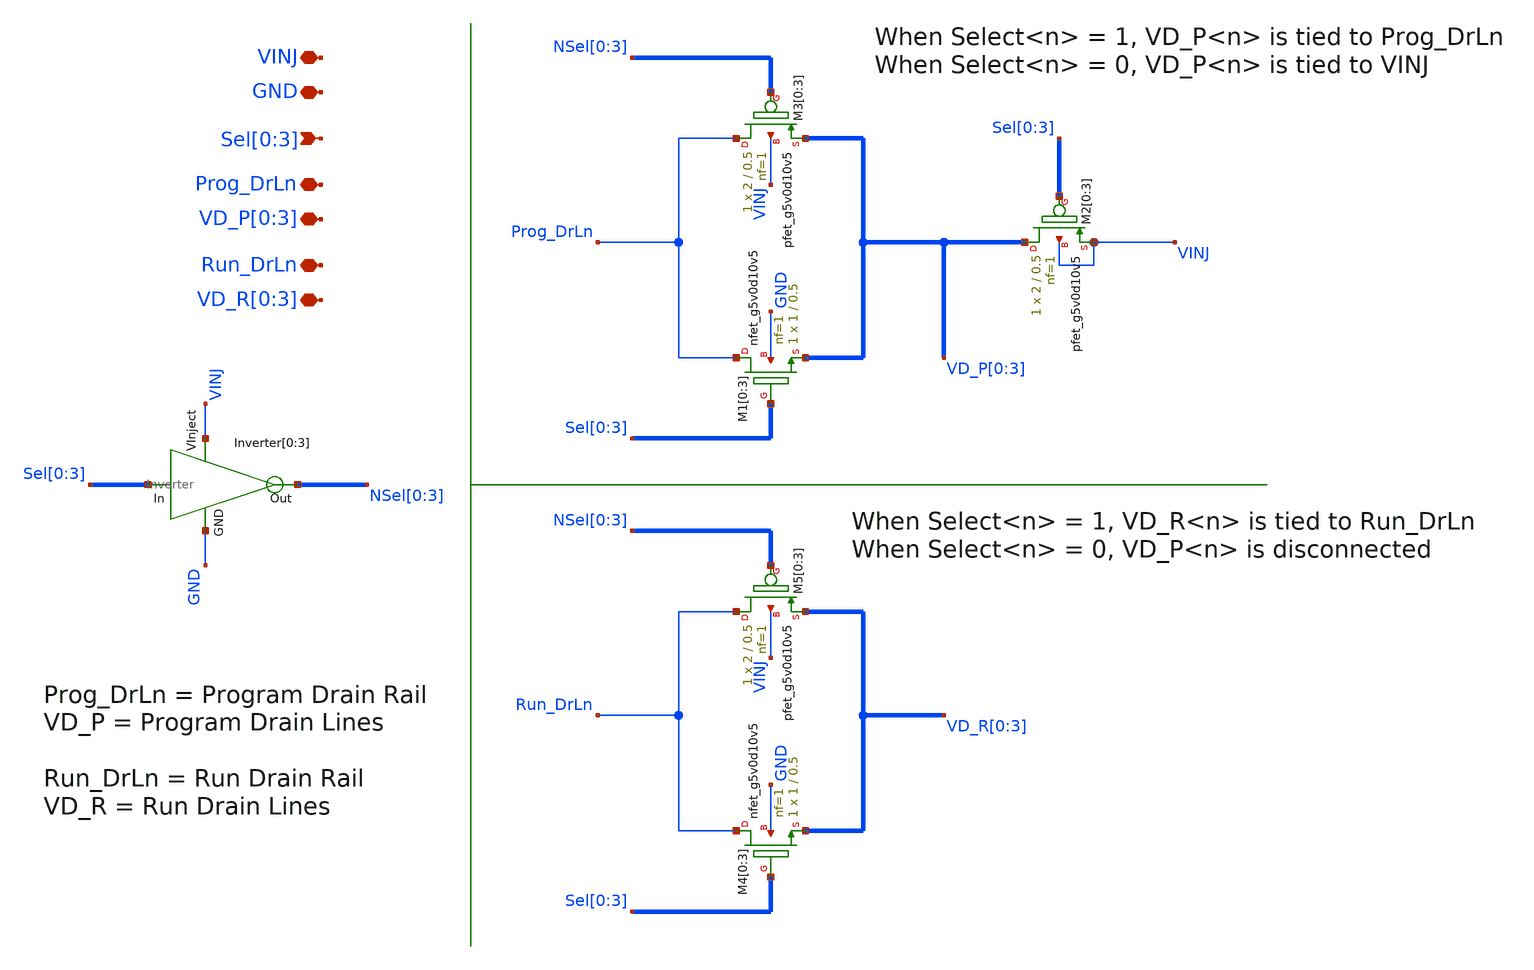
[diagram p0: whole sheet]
** sch_path: sky130_cells/IndirectVMM_DrainSwcs/IndirectVMM_DrainSwcs.sch
**.subckt IndirectVMM_DrainSwcs Sel[0],Sel[1],Sel[2],Sel[3] Prog_DrLn Run_DrLn
*+ VD_P[0],VD_P[1],VD_P[2],VD_P[3] VD_R[0],VD_R[1],VD_R[2],VD_R[3] VINJ GND
*.ipin Sel[0],Sel[1],Sel[2],Sel[3]
*.iopin Prog_DrLn
*.iopin Run_DrLn
*.iopin VD_P[0],VD_P[1],VD_P[2],VD_P[3]
*.iopin VD_R[0],VD_R[1],VD_R[2],VD_R[3]
*.iopin VINJ
*.iopin GND
Inverter[0] VINJ Sel[0] NSel[0] GND Inverter
Inverter[1] VINJ Sel[1] NSel[1] GND Inverter
Inverter[2] VINJ Sel[2] NSel[2] GND Inverter
Inverter[3] VINJ Sel[3] NSel[3] GND Inverter
XM1[0] Prog_DrLn Sel[0] VD_P[0] GND sky130_fd_pr__nfet_g5v0d10v5 L=0.5 W=1 nf=1 ad='int((1 + 1)/2) * 1 / 1 * 0.29'
+ as='int((1 + 2)/2) * 1 / 1 * 0.29' pd='2*int((1 + 1)/2) * (1 / 1 + 0.29)' ps='2*int((1 + 2)/2) * (1 / 1 + 0.29)'
+ nrd='0.29 / 1 ' nrs='0.29 / 1 ' sa=0 sb=0 sd=0 mult=1 m=1
XM1[1] Prog_DrLn Sel[1] VD_P[1] GND sky130_fd_pr__nfet_g5v0d10v5 L=0.5 W=1 nf=1 ad='int((1 + 1)/2) * 1 / 1 * 0.29'
+ as='int((1 + 2)/2) * 1 / 1 * 0.29' pd='2*int((1 + 1)/2) * (1 / 1 + 0.29)' ps='2*int((1 + 2)/2) * (1 / 1 + 0.29)'
+ nrd='0.29 / 1 ' nrs='0.29 / 1 ' sa=0 sb=0 sd=0 mult=1 m=1
XM1[2] Prog_DrLn Sel[2] VD_P[2] GND sky130_fd_pr__nfet_g5v0d10v5 L=0.5 W=1 nf=1 ad='int((1 + 1)/2) * 1 / 1 * 0.29'
+ as='int((1 + 2)/2) * 1 / 1 * 0.29' pd='2*int((1 + 1)/2) * (1 / 1 + 0.29)' ps='2*int((1 + 2)/2) * (1 / 1 + 0.29)'
+ nrd='0.29 / 1 ' nrs='0.29 / 1 ' sa=0 sb=0 sd=0 mult=1 m=1
XM1[3] Prog_DrLn Sel[3] VD_P[3] GND sky130_fd_pr__nfet_g5v0d10v5 L=0.5 W=1 nf=1 ad='int((1 + 1)/2) * 1 / 1 * 0.29'
+ as='int((1 + 2)/2) * 1 / 1 * 0.29' pd='2*int((1 + 1)/2) * (1 / 1 + 0.29)' ps='2*int((1 + 2)/2) * (1 / 1 + 0.29)'
+ nrd='0.29 / 1 ' nrs='0.29 / 1 ' sa=0 sb=0 sd=0 mult=1 m=1
XM2[0] VD_P[0] Sel[0] VINJ VINJ sky130_fd_pr__pfet_g5v0d10v5 L=0.5 W=2 nf=1 ad='int((1 + 1)/2) * 2 / 1 * 0.29'
+ as='int((1 + 2)/2) * 2 / 1 * 0.29' pd='2*int((1 + 1)/2) * (2 / 1 + 0.29)' ps='2*int((1 + 2)/2) * (2 / 1 + 0.29)'
+ nrd='0.29 / 2 ' nrs='0.29 / 2 ' sa=0 sb=0 sd=0 mult=1 m=1
XM2[1] VD_P[1] Sel[1] VINJ VINJ sky130_fd_pr__pfet_g5v0d10v5 L=0.5 W=2 nf=1 ad='int((1 + 1)/2) * 2 / 1 * 0.29'
+ as='int((1 + 2)/2) * 2 / 1 * 0.29' pd='2*int((1 + 1)/2) * (2 / 1 + 0.29)' ps='2*int((1 + 2)/2) * (2 / 1 + 0.29)'
+ nrd='0.29 / 2 ' nrs='0.29 / 2 ' sa=0 sb=0 sd=0 mult=1 m=1
XM2[2] VD_P[2] Sel[2] VINJ VINJ sky130_fd_pr__pfet_g5v0d10v5 L=0.5 W=2 nf=1 ad='int((1 + 1)/2) * 2 / 1 * 0.29'
+ as='int((1 + 2)/2) * 2 / 1 * 0.29' pd='2*int((1 + 1)/2) * (2 / 1 + 0.29)' ps='2*int((1 + 2)/2) * (2 / 1 + 0.29)'
+ nrd='0.29 / 2 ' nrs='0.29 / 2 ' sa=0 sb=0 sd=0 mult=1 m=1
XM2[3] VD_P[3] Sel[3] VINJ VINJ sky130_fd_pr__pfet_g5v0d10v5 L=0.5 W=2 nf=1 ad='int((1 + 1)/2) * 2 / 1 * 0.29'
+ as='int((1 + 2)/2) * 2 / 1 * 0.29' pd='2*int((1 + 1)/2) * (2 / 1 + 0.29)' ps='2*int((1 + 2)/2) * (2 / 1 + 0.29)'
+ nrd='0.29 / 2 ' nrs='0.29 / 2 ' sa=0 sb=0 sd=0 mult=1 m=1
XM3[0] Prog_DrLn NSel[0] VD_P[0] VINJ sky130_fd_pr__pfet_g5v0d10v5 L=0.5 W=2 nf=1 ad='int((1 + 1)/2) * 2 / 1 * 0.29'
+ as='int((1 + 2)/2) * 2 / 1 * 0.29' pd='2*int((1 + 1)/2) * (2 / 1 + 0.29)' ps='2*int((1 + 2)/2) * (2 / 1 + 0.29)'
+ nrd='0.29 / 2 ' nrs='0.29 / 2 ' sa=0 sb=0 sd=0 mult=1 m=1
XM3[1] Prog_DrLn NSel[1] VD_P[1] VINJ sky130_fd_pr__pfet_g5v0d10v5 L=0.5 W=2 nf=1 ad='int((1 + 1)/2) * 2 / 1 * 0.29'
+ as='int((1 + 2)/2) * 2 / 1 * 0.29' pd='2*int((1 + 1)/2) * (2 / 1 + 0.29)' ps='2*int((1 + 2)/2) * (2 / 1 + 0.29)'
+ nrd='0.29 / 2 ' nrs='0.29 / 2 ' sa=0 sb=0 sd=0 mult=1 m=1
XM3[2] Prog_DrLn NSel[2] VD_P[2] VINJ sky130_fd_pr__pfet_g5v0d10v5 L=0.5 W=2 nf=1 ad='int((1 + 1)/2) * 2 / 1 * 0.29'
+ as='int((1 + 2)/2) * 2 / 1 * 0.29' pd='2*int((1 + 1)/2) * (2 / 1 + 0.29)' ps='2*int((1 + 2)/2) * (2 / 1 + 0.29)'
+ nrd='0.29 / 2 ' nrs='0.29 / 2 ' sa=0 sb=0 sd=0 mult=1 m=1
XM3[3] Prog_DrLn NSel[3] VD_P[3] VINJ sky130_fd_pr__pfet_g5v0d10v5 L=0.5 W=2 nf=1 ad='int((1 + 1)/2) * 2 / 1 * 0.29'
+ as='int((1 + 2)/2) * 2 / 1 * 0.29' pd='2*int((1 + 1)/2) * (2 / 1 + 0.29)' ps='2*int((1 + 2)/2) * (2 / 1 + 0.29)'
+ nrd='0.29 / 2 ' nrs='0.29 / 2 ' sa=0 sb=0 sd=0 mult=1 m=1
XM4[0] Run_DrLn Sel[0] VD_R[0] GND sky130_fd_pr__nfet_g5v0d10v5 L=0.5 W=1 nf=1 ad='int((1 + 1)/2) * 1 / 1 * 0.29'
+ as='int((1 + 2)/2) * 1 / 1 * 0.29' pd='2*int((1 + 1)/2) * (1 / 1 + 0.29)' ps='2*int((1 + 2)/2) * (1 / 1 + 0.29)'
+ nrd='0.29 / 1 ' nrs='0.29 / 1 ' sa=0 sb=0 sd=0 mult=1 m=1
XM4[1] Run_DrLn Sel[1] VD_R[1] GND sky130_fd_pr__nfet_g5v0d10v5 L=0.5 W=1 nf=1 ad='int((1 + 1)/2) * 1 / 1 * 0.29'
+ as='int((1 + 2)/2) * 1 / 1 * 0.29' pd='2*int((1 + 1)/2) * (1 / 1 + 0.29)' ps='2*int((1 + 2)/2) * (1 / 1 + 0.29)'
+ nrd='0.29 / 1 ' nrs='0.29 / 1 ' sa=0 sb=0 sd=0 mult=1 m=1
XM4[2] Run_DrLn Sel[2] VD_R[2] GND sky130_fd_pr__nfet_g5v0d10v5 L=0.5 W=1 nf=1 ad='int((1 + 1)/2) * 1 / 1 * 0.29'
+ as='int((1 + 2)/2) * 1 / 1 * 0.29' pd='2*int((1 + 1)/2) * (1 / 1 + 0.29)' ps='2*int((1 + 2)/2) * (1 / 1 + 0.29)'
+ nrd='0.29 / 1 ' nrs='0.29 / 1 ' sa=0 sb=0 sd=0 mult=1 m=1
XM4[3] Run_DrLn Sel[3] VD_R[3] GND sky130_fd_pr__nfet_g5v0d10v5 L=0.5 W=1 nf=1 ad='int((1 + 1)/2) * 1 / 1 * 0.29'
+ as='int((1 + 2)/2) * 1 / 1 * 0.29' pd='2*int((1 + 1)/2) * (1 / 1 + 0.29)' ps='2*int((1 + 2)/2) * (1 / 1 + 0.29)'
+ nrd='0.29 / 1 ' nrs='0.29 / 1 ' sa=0 sb=0 sd=0 mult=1 m=1
XM5[0] Run_DrLn NSel[0] VD_R[0] VINJ sky130_fd_pr__pfet_g5v0d10v5 L=0.5 W=2 nf=1 ad='int((1 + 1)/2) * 2 / 1 * 0.29'
+ as='int((1 + 2)/2) * 2 / 1 * 0.29' pd='2*int((1 + 1)/2) * (2 / 1 + 0.29)' ps='2*int((1 + 2)/2) * (2 / 1 + 0.29)'
+ nrd='0.29 / 2 ' nrs='0.29 / 2 ' sa=0 sb=0 sd=0 mult=1 m=1
XM5[1] Run_DrLn NSel[1] VD_R[1] VINJ sky130_fd_pr__pfet_g5v0d10v5 L=0.5 W=2 nf=1 ad='int((1 + 1)/2) * 2 / 1 * 0.29'
+ as='int((1 + 2)/2) * 2 / 1 * 0.29' pd='2*int((1 + 1)/2) * (2 / 1 + 0.29)' ps='2*int((1 + 2)/2) * (2 / 1 + 0.29)'
+ nrd='0.29 / 2 ' nrs='0.29 / 2 ' sa=0 sb=0 sd=0 mult=1 m=1
XM5[2] Run_DrLn NSel[2] VD_R[2] VINJ sky130_fd_pr__pfet_g5v0d10v5 L=0.5 W=2 nf=1 ad='int((1 + 1)/2) * 2 / 1 * 0.29'
+ as='int((1 + 2)/2) * 2 / 1 * 0.29' pd='2*int((1 + 1)/2) * (2 / 1 + 0.29)' ps='2*int((1 + 2)/2) * (2 / 1 + 0.29)'
+ nrd='0.29 / 2 ' nrs='0.29 / 2 ' sa=0 sb=0 sd=0 mult=1 m=1
XM5[3] Run_DrLn NSel[3] VD_R[3] VINJ sky130_fd_pr__pfet_g5v0d10v5 L=0.5 W=2 nf=1 ad='int((1 + 1)/2) * 2 / 1 * 0.29'
+ as='int((1 + 2)/2) * 2 / 1 * 0.29' pd='2*int((1 + 1)/2) * (2 / 1 + 0.29)' ps='2*int((1 + 2)/2) * (2 / 1 + 0.29)'
+ nrd='0.29 / 2 ' nrs='0.29 / 2 ' sa=0 sb=0 sd=0 mult=1 m=1
**.ends

* expanding   symbol:  sky130_cells/IndirectVMM_DrainSwcs/Inverter.sym # of pins=4
** sym_path: sky130_cells/IndirectVMM_DrainSwcs/Inverter.sym
** sch_path: sky130_cells/IndirectVMM_DrainSwcs/Inverter.sch
.subckt Inverter VInject In Out GND
*.ipin In
*.ipin VInject
*.ipin GND
*.opin Out
XM1 Out In GND GND sky130_fd_pr__nfet_g5v0d10v5 L=0.5 W=0.5 nf=1 ad='int((1 + 1)/2) * 0.5 / 1 * 0.29'
+ as='int((1 + 2)/2) * 0.5 / 1 * 0.29' pd='2*int((1 + 1)/2) * (0.5 / 1 + 0.29)' ps='2*int((1 + 2)/2) * (0.5 / 1 + 0.29)'
+ nrd='0.29 / 0.5 ' nrs='0.29 / 0.5 ' sa=0 sb=0 sd=0 mult=1 m=1
XM2 Out In VInject VInject sky130_fd_pr__pfet_g5v0d10v5 L=0.5 W=1 nf=1 ad='int((1 + 1)/2) * 1 / 1 * 0.29'
+ as='int((1 + 2)/2) * 1 / 1 * 0.29' pd='2*int((1 + 1)/2) * (1 / 1 + 0.29)' ps='2*int((1 + 2)/2) * (1 / 1 + 0.29)'
+ nrd='0.29 / 1 ' nrs='0.29 / 1 ' sa=0 sb=0 sd=0 mult=1 m=1
.ends

.end
